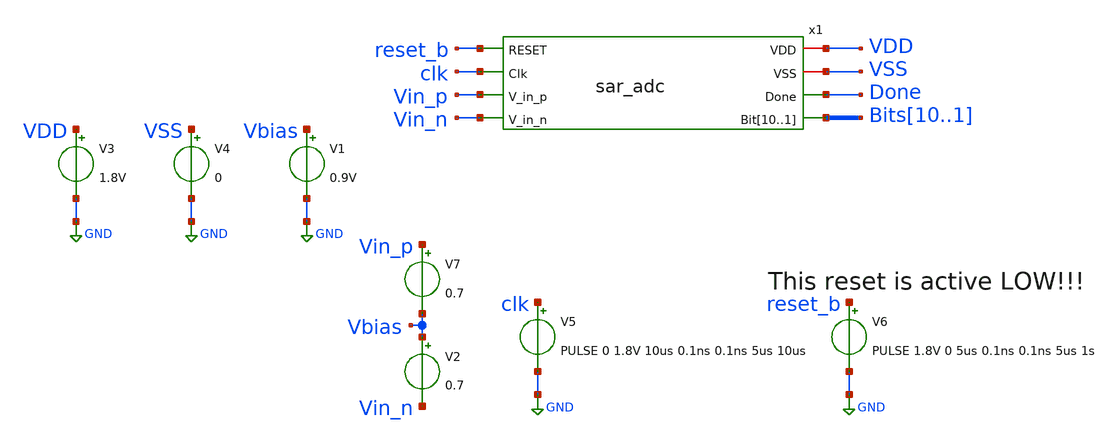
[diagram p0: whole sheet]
** sch_path: xschem/tests/sar_adc/sar_adc_test.sch
**.subckt sar_adc_test
V3 VDD GND 1.8V
V4 VSS GND 0
x1 VDD VSS reset_b clk Vin_p Vin_n Done Bits10 Bits9 Bits8 Bits7 Bits6 Bits5 Bits4 Bits3 Bits2 Bits1
+ sar_adc
V2 Vbias Vin_n 0.7
V5 clk GND PULSE 0 1.8V 10us 0.1ns 0.1ns 5us 10us
V6 reset_b GND PULSE 1.8V 0 5us 0.1ns 0.1ns 5us 1s
V1 Vbias GND 0.9V
V7 Vin_p Vbias 0.7
**** begin user architecture code
 .lib $::SKYWATER_MODELS/sky130.lib.spice tt
.include $::SKYWATER_STDCELLS/sky130_fd_sc_hd.spice


.options acct list
.temp 25
*vvcc VDD 0 dc 1.8
*vvss VSS 0 0
.ic v(x1.vsampled_p)=0.9V v(x1.vsampled_n)=0.9V
.control
tran 0.05u 400u
*plot RST_PLS clk+2 Pulse+4
plot Done-4 Vin_p-Vin_n-2 bits1 bits2+2 bits3+4 bits4+6 bits5+8 bits6+10 bits7+12 bits8+14 bits9+16
+ bits10+18
plot x1.vsampled_p x1.vsampled_n x1.vsampled_p-x1.vsampled_n x1.sw_sample-2 x1.comp_out_p+2
write sar_adc_test.raw
.endc


**** end user architecture code
**.ends
.GLOBAL GND
.end
